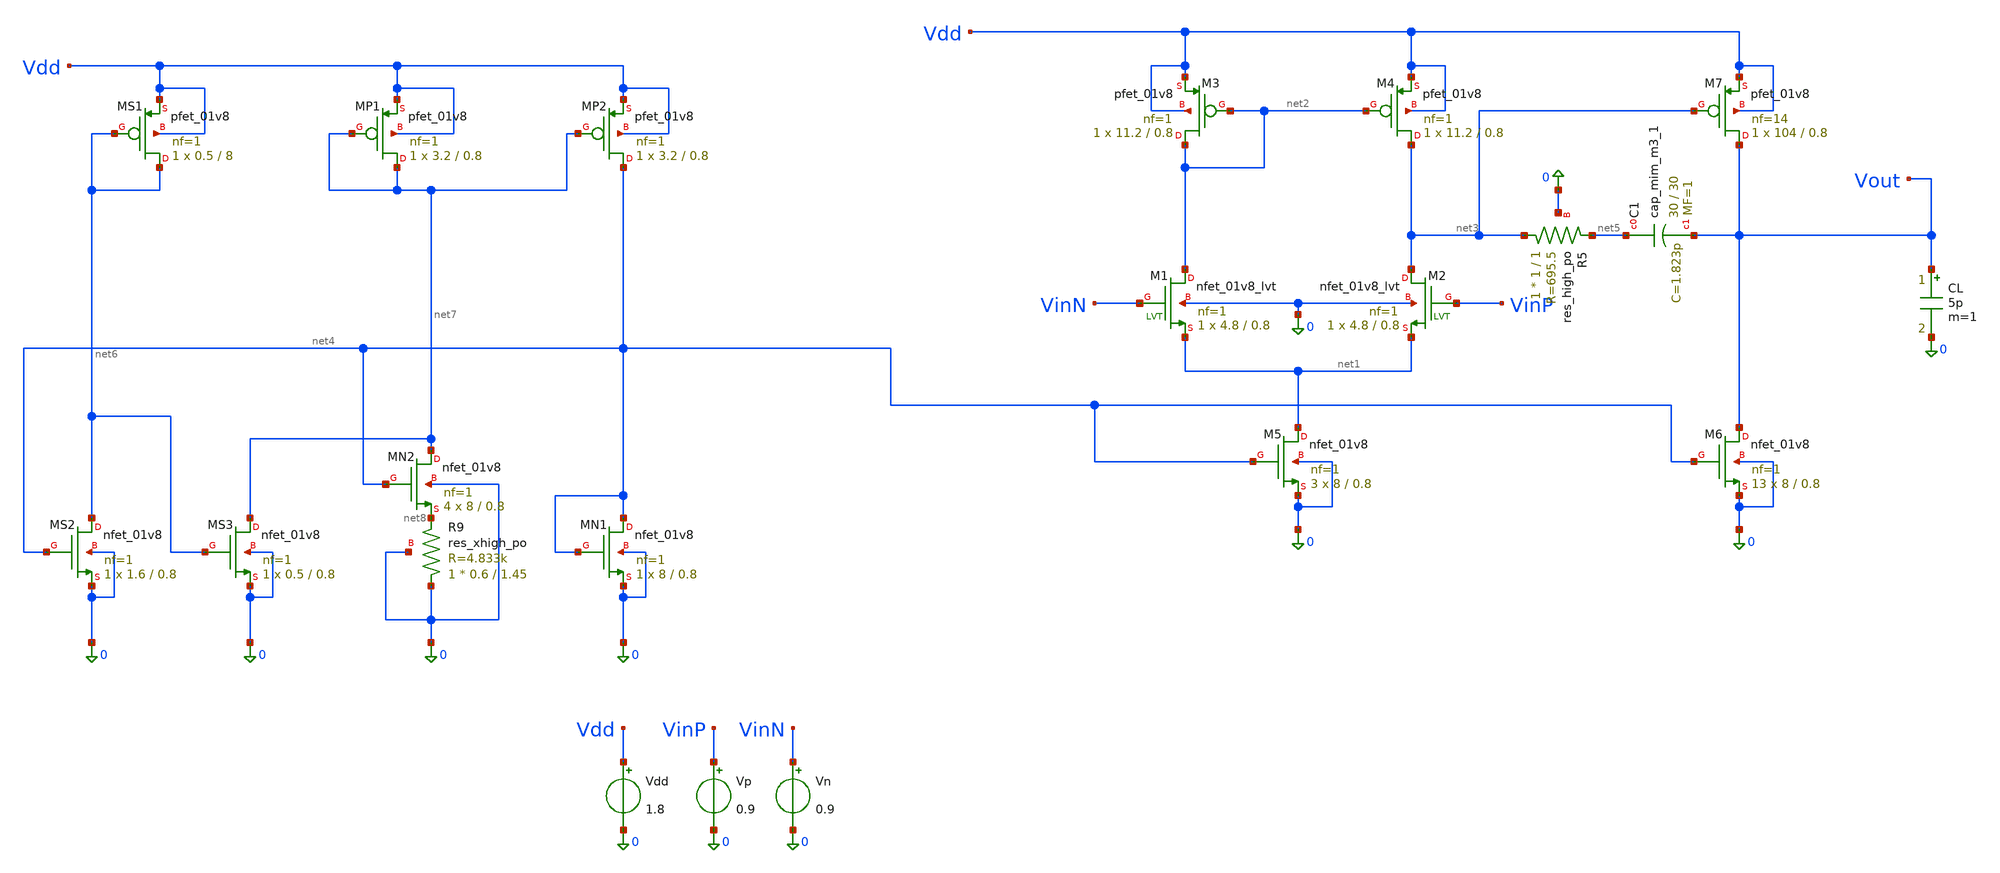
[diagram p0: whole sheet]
** sch_path: parameter_extraction/opamp.sch
**.subckt opamp
XM1 net2 VinN net1 0 sky130_fd_pr__nfet_01v8_lvt L=0.8 W=4.8 nf=1 ad='int((1 + 1)/2) * 4.8 / 1 * 0.29'
+ as='int((1 + 2)/2) * 4.8 / 1 * 0.29' pd='2*int((1 + 1)/2) * (4.8 / 1 + 0.29)' ps='2*int((1 + 2)/2) * (4.8 / 1 + 0.29)'
+ nrd='0.29 / 4.8 ' nrs='0.29 / 4.8 ' sa=0 sb=0 sd=0 mult=1 m=1
XM3 net2 net2 Vdd Vdd sky130_fd_pr__pfet_01v8 L=0.8 W=11.2 nf=1 ad='int((1 + 1)/2) * 11.2 / 1 * 0.29'
+ as='int((1 + 2)/2) * 11.2 / 1 * 0.29' pd='2*int((1 + 1)/2) * (11.2 / 1 + 0.29)' ps='2*int((1 + 2)/2) * (11.2 / 1 + 0.29)'
+ nrd='0.29 / 11.2 ' nrs='0.29 / 11.2 ' sa=0 sb=0 sd=0 mult=1 m=1
XM5 net1 net4 0 0 sky130_fd_pr__nfet_01v8 L=0.8 W=8 nf=1 ad='int((1 + 1)/2) * 8 / 1 * 0.29' as='int((1 + 2)/2) * 8 / 1 * 0.29'
+ pd='2*int((1 + 1)/2) * (8 / 1 + 0.29)' ps='2*int((1 + 2)/2) * (8 / 1 + 0.29)' nrd='0.29 / 8 ' nrs='0.29 / 8 '
+ sa=0 sb=0 sd=0 mult=3 m=3
XM2 net3 VinP net1 0 sky130_fd_pr__nfet_01v8_lvt L=0.8 W=4.8 nf=1 ad='int((1 + 1)/2) * 4.8 / 1 * 0.29'
+ as='int((1 + 2)/2) * 4.8 / 1 * 0.29' pd='2*int((1 + 1)/2) * (4.8 / 1 + 0.29)' ps='2*int((1 + 2)/2) * (4.8 / 1 + 0.29)'
+ nrd='0.29 / 4.8 ' nrs='0.29 / 4.8 ' sa=0 sb=0 sd=0 mult=1 m=1
XM4 net3 net2 Vdd Vdd sky130_fd_pr__pfet_01v8 L=0.8 W=11.2 nf=1 ad='int((1 + 1)/2) * 11.2 / 1 * 0.29'
+ as='int((1 + 2)/2) * 11.2 / 1 * 0.29' pd='2*int((1 + 1)/2) * (11.2 / 1 + 0.29)' ps='2*int((1 + 2)/2) * (11.2 / 1 + 0.29)'
+ nrd='0.29 / 11.2 ' nrs='0.29 / 11.2 ' sa=0 sb=0 sd=0 mult=1 m=1
XM6 Vout net4 0 0 sky130_fd_pr__nfet_01v8 L=0.8 W=8 nf=1 ad='int((1 + 1)/2) * 8 / 1 * 0.29' as='int((1 + 2)/2) * 8 / 1 * 0.29'
+ pd='2*int((1 + 1)/2) * (8 / 1 + 0.29)' ps='2*int((1 + 2)/2) * (8 / 1 + 0.29)' nrd='0.29 / 8 ' nrs='0.29 / 8 '
+ sa=0 sb=0 sd=0 mult=13 m=13
XM7 Vout net3 Vdd Vdd sky130_fd_pr__pfet_01v8 L=0.8 W=104 nf=14 ad='int((14 + 1)/2) * 104 / 14 * 0.29'
+ as='int((14 + 2)/2) * 104 / 14 * 0.29' pd='2*int((14 + 1)/2) * (104 / 14 + 0.29)' ps='2*int((14 + 2)/2) * (104 / 14 + 0.29)'
+ nrd='0.29 / 104 ' nrs='0.29 / 104 ' sa=0 sb=0 sd=0 mult=1 m=1
XC1 net5 Vout sky130_fd_pr__cap_mim_m3_1 W=30 L=30 MF=1 m=1
Vdd Vdd 0 1.8
Vp VinP 0 0.9
Vn VinN 0 0.9
XR5 net3 net5 0 sky130_fd_pr__res_high_po W=1 L=1 mult=1 m=1
CL Vout 0 5p m=1
XMS1 net6 net6 Vdd Vdd sky130_fd_pr__pfet_01v8 L=8 W=0.5 nf=1 ad='int((1 + 1)/2) * 0.5 / 1 * 0.29' as='int((1 + 2)/2) * 0.5 / 1 * 0.29'
+ pd='2*int((1 + 1)/2) * (0.5 / 1 + 0.29)' ps='2*int((1 + 2)/2) * (0.5 / 1 + 0.29)' nrd='0.29 / 0.5 ' nrs='0.29 / 0.5 '
+ sa=0 sb=0 sd=0 mult=1 m=1
XMP1 net7 net7 Vdd Vdd sky130_fd_pr__pfet_01v8 L=0.8 W=3.2 nf=1 ad='int((1 + 1)/2) * 3.2 / 1 * 0.29'
+ as='int((1 + 2)/2) * 3.2 / 1 * 0.29' pd='2*int((1 + 1)/2) * (3.2 / 1 + 0.29)' ps='2*int((1 + 2)/2) * (3.2 / 1 + 0.29)'
+ nrd='0.29 / 3.2 ' nrs='0.29 / 3.2 ' sa=0 sb=0 sd=0 mult=1 m=1
XMP2 net4 net7 Vdd Vdd sky130_fd_pr__pfet_01v8 L=0.8 W=3.2 nf=1 ad='int((1 + 1)/2) * 3.2 / 1 * 0.29'
+ as='int((1 + 2)/2) * 3.2 / 1 * 0.29' pd='2*int((1 + 1)/2) * (3.2 / 1 + 0.29)' ps='2*int((1 + 2)/2) * (3.2 / 1 + 0.29)'
+ nrd='0.29 / 3.2 ' nrs='0.29 / 3.2 ' sa=0 sb=0 sd=0 mult=1 m=1
XR9 0 net8 0 sky130_fd_pr__res_xhigh_po W=0.6 L=1.45 mult=1 m=1
XMS2 net6 net4 0 0 sky130_fd_pr__nfet_01v8 L=0.8 W=1.6 nf=1 ad='int((1 + 1)/2) * 1.6 / 1 * 0.29' as='int((1 + 2)/2) * 1.6 / 1 * 0.29'
+ pd='2*int((1 + 1)/2) * (1.6 / 1 + 0.29)' ps='2*int((1 + 2)/2) * (1.6 / 1 + 0.29)' nrd='0.29 / 1.6 ' nrs='0.29 / 1.6 '
+ sa=0 sb=0 sd=0 mult=1 m=1
XMS3 net7 net6 0 0 sky130_fd_pr__nfet_01v8 L=0.8 W=0.5 nf=1 ad='int((1 + 1)/2) * 0.5 / 1 * 0.29' as='int((1 + 2)/2) * 0.5 / 1 * 0.29'
+ pd='2*int((1 + 1)/2) * (0.5 / 1 + 0.29)' ps='2*int((1 + 2)/2) * (0.5 / 1 + 0.29)' nrd='0.29 / 0.5 ' nrs='0.29 / 0.5 '
+ sa=0 sb=0 sd=0 mult=1 m=1
XMN2 net7 net4 net8 0 sky130_fd_pr__nfet_01v8 L=0.8 W=8 nf=1 ad='int((1 + 1)/2) * 8 / 1 * 0.29' as='int((1 + 2)/2) * 8 / 1 * 0.29'
+ pd='2*int((1 + 1)/2) * (8 / 1 + 0.29)' ps='2*int((1 + 2)/2) * (8 / 1 + 0.29)' nrd='0.29 / 8 ' nrs='0.29 / 8 '
+ sa=0 sb=0 sd=0 mult=4 m=4
XMN1 net4 net4 0 0 sky130_fd_pr__nfet_01v8 L=0.8 W=8 nf=1 ad='int((1 + 1)/2) * 8 / 1 * 0.29' as='int((1 + 2)/2) * 8 / 1 * 0.29'
+ pd='2*int((1 + 1)/2) * (8 / 1 + 0.29)' ps='2*int((1 + 2)/2) * (8 / 1 + 0.29)' nrd='0.29 / 8 ' nrs='0.29 / 8 '
+ sa=0 sb=0 sd=0 mult=1 m=1
**** begin user architecture code


.lib /foss/pdks/sky130A/libs.tech/combined/sky130.lib.spice tt
.option rshunt=1e12
.control
* ================= user settings =================
* name of the supply source and of the load capacitor in your schematic
set vddsrc = Vdd
set clname = CL
let vref = 0.9
* load capacitances for the stability sweep
set cllist = ( 0.5p 1p 2p 5p )
* common-mode voltages for the ICMR test
set vcmlist = ( 0.6 0.7 0.75 0.8 0.85 0.9 1.0 1.1 1.15 1.2 1.3 )
* internal names of M1 (input), M3 (mirror) and M5 (tail), as printed by 'show' in test 1
set m1 = m.xm1.msky130_fd_pr__nfet_01v8_lvt
set m5 = m.xm5.msky130_fd_pr__nfet_01v8
* ==================================================
set color0=white
set xbrushwidth=2





echo
echo ========== 1) DC operating point ==========
alter Vp dc=0.9
alter Vn dc=0.9
op
echo Check every transistor: vds must be larger than vdsat (saturation)
show m : id vgs vds vdsat gm gds
let itot_ua = -i($vddsrc)*1e6
echo Total supply current (uA) = $&itot_ua

echo
echo ========== 2) Offset, DC transfer, output swing ==========
alter Vn dc=0.9
dc Vp 0.88 0.92 1u
let vin_bal = vref
meas dc vbal find v(vinp) when v(vout)=0.9
let vos_mv = (vbal - 0.9)*1e3
echo Systematic input offset (mV) = $&vos_mv
let vd    = (v(vinp) - 0.9)*1e3
let gain  = deriv(v(vout))
let gaindb = db(abs(gain)+1e-12)
plot v(vout) vs vd xlabel 'Vp - Vn (mV)' ylabel 'Vout (V)' title 'Open-loop DC transfer'
plot gaindb vs v(vout) xlimit 0 1.8 xlabel 'Vout (V)' ylabel 'dVout/dVin (dB)' title 'Gain vs output voltage (swing = where it stays high)'

echo
echo ========== 3) Open-loop AC: A0, GBW, PM, GM ==========
alter Vp dc=$&vbal
alter Vp ac=1
alter Vn ac=0
ac dec 50 1 1G
let ph = 180/pi*cph(v(vout))
meas ac A0db  find vdb(vout) at=1
meas ac ph1 find ph at=1
echo Phase at 1 Hz = $&ph1 deg  (must be near 0. Near +-180 means VinP and VinN are swapped)
meas ac fugf  when vdb(vout)=0
meas ac phu   find ph at=fugf
let pm = 180 + phu
meas ac f180 when ph=-180
meas ac gmdb find vdb(vout) at=f180
set a0 = $&A0db
echo A0 = $&A0db dB, GBW = $&fugf Hz, PM = $&pm deg, GM = $&gmdb dB (negative = margin)
plot vdb(vout) xlog ylabel 'Gain (dB)' title 'Open-loop gain'
plot ph xlog ylabel 'Phase (deg)' title 'Open-loop phase'

echo
echo ========== 4) Stability vs load capacitance ==========
foreach cl $cllist
  alter $clname c=$cl
  ac dec 50 1 1G
  let ph = 180/pi*cph(v(vout))
  meas ac fu when vdb(vout)=0
  meas ac phx find ph at=fu
  let pmx = 180 + phx
  echo CL = $cl : GBW = $&fu Hz, PM = $&pmx deg
end
alter $clname c=5p

echo
echo ========== 5) CMRR and PSRR (at 1 Hz) ==========
alter Vp ac=1
alter Vn ac=1
ac dec 20 1 100Meg
meas ac acm1 find vdb(vout) at=1
let cmrr = $a0 - acm1
echo CMRR at 1 Hz = $&cmrr dB
alter Vp ac=0
alter Vn ac=0
alter $vddsrc ac=1
ac dec 20 1 100Meg
meas ac avdd1 find vdb(vout) at=1
let psrr = $a0 - avdd1
echo PSRR+ at 1 Hz = $&psrr dB
alter $vddsrc ac=0
alter Vp ac=1

echo
echo ========== 6) Input-referred noise ==========
noise v(vout) Vp dec 20 1 100Meg
echo current plot: $curplot
setplot previous
echo spectrum plot: $curplot
let vn1k   = inoise_spectrum[60]*1e9
let vn100k = inoise_spectrum[100]*1e9
echo Input noise: $&vn1k nV/rtHz at 1 kHz, $&vn100k nV/rtHz at 100 kHz
plot inoise_spectrum xlog ylog ylabel 'V/sqrt(Hz)' title 'Input-referred noise density'

echo
echo ========== 7) ICMR: open-loop gain vs common-mode voltage ==========
foreach vc $vcmlist
  alter Vn dc=$vc
  let lo = $vc - 0.03
  let hi = $vc + 0.03
  dc Vp $&lo $&hi 2u
  meas dc vb find v(vinp) when v(vout)=0.9
  alter Vp dc=$&vb
  op
  let mg1 = (@{$m1}[vds] - @{$m1}[vdsat])*1e3
  let mg5 = (@{$m5}[vds] - @{$m5}[vdsat])*1e3
  let itail = @{$m5}[id]*1e6
  set s1 = $&mg1
  set s5 = $&mg5
  set st = $&itail
  ac lin 1 10 10
  let a = vdb(vout)
  echo Vcm = $vc V : A0 = $&a dB, M1 vds-vdsat = $s1 mV, M5 vds-vdsat = $s5 mV, Itail = $st uA
end
alter Vn dc=0.9
.endc


**** end user architecture code
**.ends
.end
